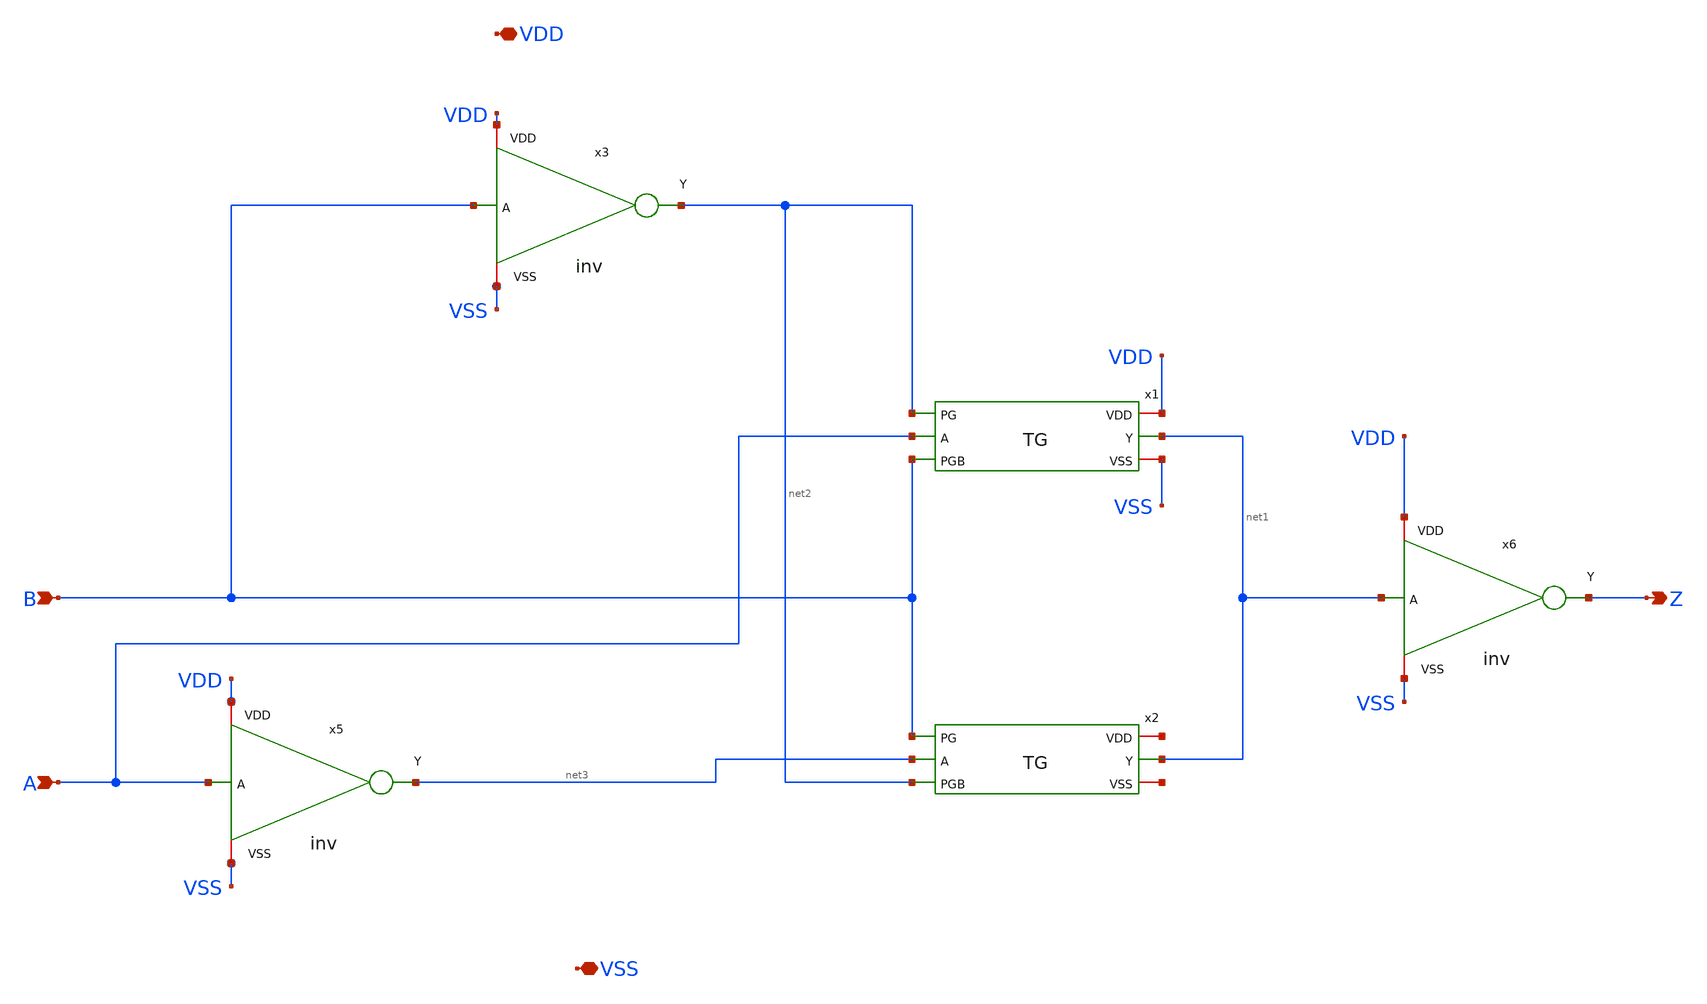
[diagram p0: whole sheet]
** sch_path: test_XOR2_1.sch
**.subckt test_XOR2_1 A B Z VDD VSS
*.ipin A
*.ipin B
*.opin Z
*.iopin VDD
*.iopin VSS
x1 net2 VDD net1 A VSS B TG
x2 B net4 net1 net3 net5 net2 TG
x3 VDD B net2 VSS inv
x5 VDD A net3 VSS inv
x6 VDD net1 Z VSS inv
**.ends
.end
